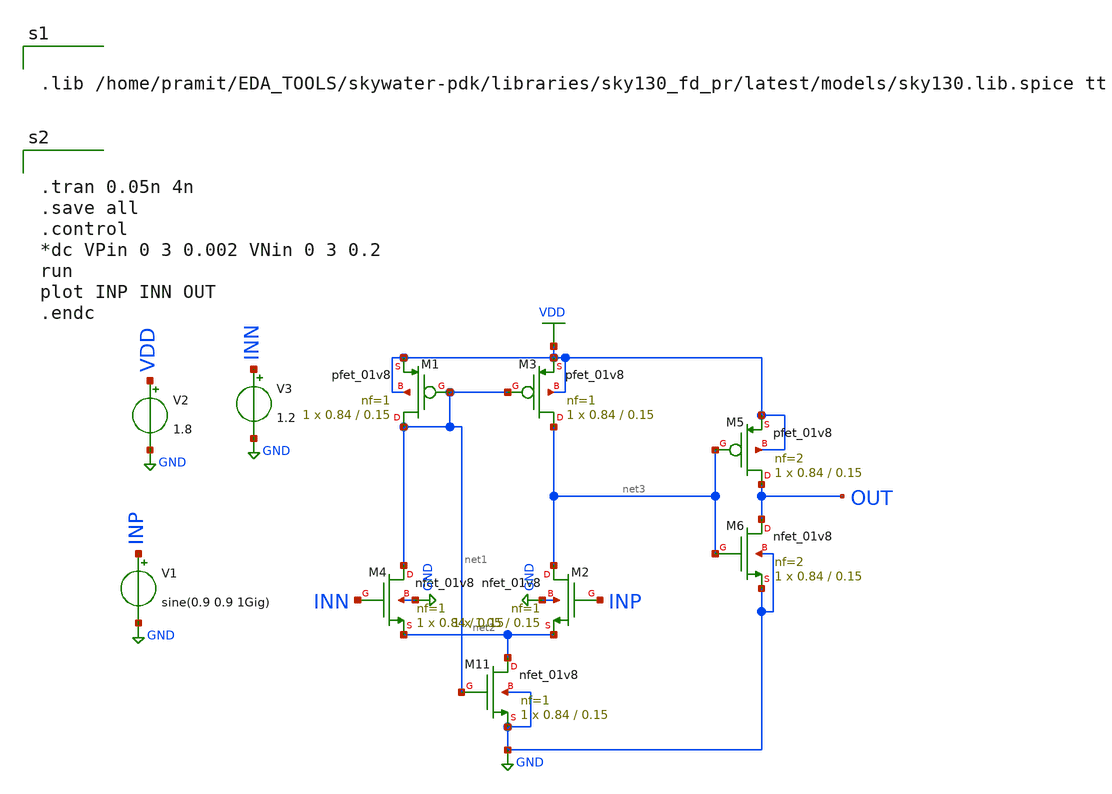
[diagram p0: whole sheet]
** sch_path: week5/ADC_layout/comparator2.sch
**.subckt comparator2
XM1 net1 net1 VDD VDD sky130_fd_pr__pfet_01v8 L=0.15 W=0.84 nf=1 ad='int((nf+1)/2) * W/nf * 0.29' as='int((nf+2)/2) * W/nf * 0.29'
+ pd='2*int((nf+1)/2) * (W/nf + 0.29)' ps='2*int((nf+2)/2) * (W/nf + 0.29)' nrd='0.29 / W' nrs='0.29 / W'
+ sa=0 sb=0 sd=0 mult=1 m=1
XM2 net3 INP net2 GND sky130_fd_pr__nfet_01v8 L=0.15 W=1.05 nf=1 ad='int((nf+1)/2) * W/nf * 0.29' as='int((nf+2)/2) * W/nf * 0.29'
+ pd='2*int((nf+1)/2) * (W/nf + 0.29)' ps='2*int((nf+2)/2) * (W/nf + 0.29)' nrd='0.29 / W' nrs='0.29 / W'
+ sa=0 sb=0 sd=0 mult=1 m=1
XM3 net3 net1 VDD VDD sky130_fd_pr__pfet_01v8 L=0.15 W=0.84 nf=1 ad='int((nf+1)/2) * W/nf * 0.29' as='int((nf+2)/2) * W/nf * 0.29'
+ pd='2*int((nf+1)/2) * (W/nf + 0.29)' ps='2*int((nf+2)/2) * (W/nf + 0.29)' nrd='0.29 / W' nrs='0.29 / W'
+ sa=0 sb=0 sd=0 mult=1 m=1
XM4 net1 INN net2 GND sky130_fd_pr__nfet_01v8 L=0.15 W=0.84 nf=1 ad='int((nf+1)/2) * W/nf * 0.29' as='int((nf+2)/2) * W/nf * 0.29'
+ pd='2*int((nf+1)/2) * (W/nf + 0.29)' ps='2*int((nf+2)/2) * (W/nf + 0.29)' nrd='0.29 / W' nrs='0.29 / W'
+ sa=0 sb=0 sd=0 mult=1 m=1
XM11 net2 net1 GND GND sky130_fd_pr__nfet_01v8 L=0.15 W=0.84 nf=1 ad='int((nf+1)/2) * W/nf * 0.29' as='int((nf+2)/2) * W/nf * 0.29'
+ pd='2*int((nf+1)/2) * (W/nf + 0.29)' ps='2*int((nf+2)/2) * (W/nf + 0.29)' nrd='0.29 / W' nrs='0.29 / W'
+ sa=0 sb=0 sd=0 mult=1 m=1
V1 INP GND sine(0.9 0.9 1Gig)
V2 VDD GND 1.8
V3 INN GND 1.2
XM5 OUT net3 VDD VDD sky130_fd_pr__pfet_01v8 L=0.15 W=0.84 nf=2 ad='int((nf+1)/2) * W/nf * 0.29' as='int((nf+2)/2) * W/nf * 0.29'
+ pd='2*int((nf+1)/2) * (W/nf + 0.29)' ps='2*int((nf+2)/2) * (W/nf + 0.29)' nrd='0.29 / W' nrs='0.29 / W'
+ sa=0 sb=0 sd=0 mult=1 m=1
XM6 OUT net3 GND GND sky130_fd_pr__nfet_01v8 L=0.15 W=0.84 nf=2 ad='int((nf+1)/2) * W/nf * 0.29' as='int((nf+2)/2) * W/nf * 0.29'
+ pd='2*int((nf+1)/2) * (W/nf + 0.29)' ps='2*int((nf+2)/2) * (W/nf + 0.29)' nrd='0.29 / W' nrs='0.29 / W'
+ sa=0 sb=0 sd=0 mult=1 m=1
**** begin user architecture code


.lib /home/pramit/EDA_TOOLS/skywater-pdk/libraries/sky130_fd_pr/latest/models/sky130.lib.spice tt



.tran 0.05n 4n
.save all
.control
*dc VPin 0 3 0.002 VNin 0 3 0.2
run
plot INP INN OUT
.endc

**** end user architecture code
**.ends
.GLOBAL VDD
.GLOBAL GND
.end
